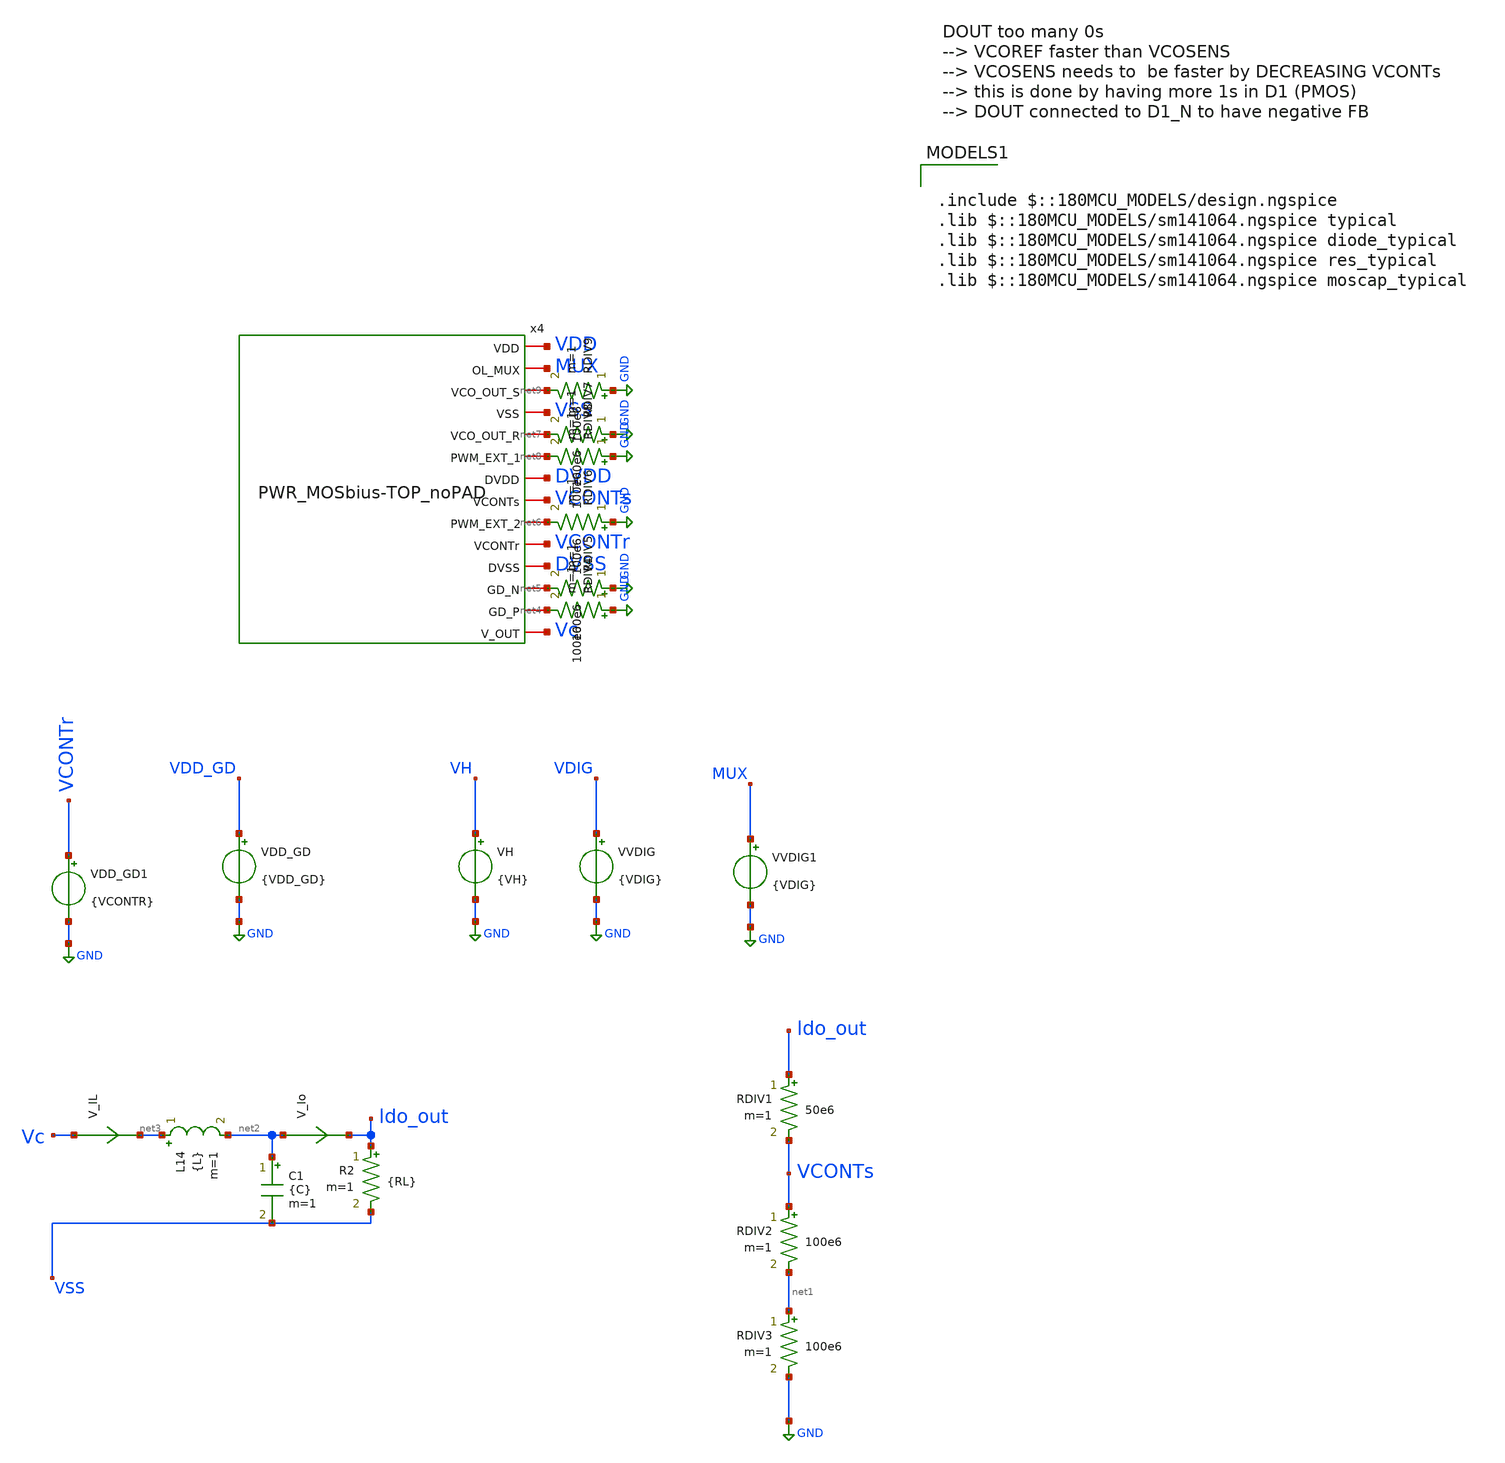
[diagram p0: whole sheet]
** sch_path: xschem/top/tb_TDBuckTOP-IHP-CL_v3p3_NOLnoPAD.sch
**.subckt tb_TDBuckTOP-IHP-CL_v3p3_NOLnoPAD
VH VH GND {VH}
VVDIG VDIG GND {VDIG}
RDIV1 ldo_out VCONTs 50e6 m=1
RDIV2 VCONTs net1 100e6 m=1
RDIV3 net1 GND 100e6 m=1
VDD_GD VDD_GD GND {VDD_GD}
L14 net3 net2 {L} m=1
C1 net2 VSS {C} m=1
V_Io net2 ldo_out 0
.save i(v_io)
V_IL Vc net3 0
.save i(v_il)
R2 ldo_out VSS {RL} m=1
VDD_GD1 VCONTr GND {VCONTR}
VVDIG1 MUX GND {VDIG}
RDIV4 GND net4 100e6 m=1
RDIV5 GND net5 100e6 m=1
RDIV6 GND net6 100e6 m=1
RDIV7 GND net7 100e6 m=1
RDIV8 GND net8 100e6 m=1
RDIV9 GND net9 100e6 m=1
x4 VDD MUX net9 VSS net7 net8 DVDD VCONTs net6 VCONTr DVSS net5 net4 Vc PWR_MOSbius-TOP_noPAD
**** begin user architecture code

.param VDIG = 5
.param VH = 5
.param VDD_GD = 5
.param VCONTR = 2
*LATEST TDBuckLOADS
*300mA
*.param RL = 6
*270mA
*.param RL = 6.67
*240mA
*.param RL = 7.5
*210mA
*.param RL = 8.57
*180mA
*.param RL = 10
*150mA
*.param RL = 12
*120mA
*.param RL = 15
*60mA
*.param RL = 30
*30mA
*.param RL = 60
*15mA
.param RL = 120
*.save v(ldo_out) v(D1) v(D1_N) v(DOUT) v(VCONTr) v(VCONTs) v(V_1r) v(V_1s) v(DOUT_buff) v(DOUT_buffn) v(vh) i(vh) v(vdd_gd) i(vdd_gd) i(v_res) v(VCONTs_OL) v(vcp) v(vcn) i(vldo_out) i(vvdig) i(vvdd)
.save all
vvdd vdd 0 dc 5
vvss vss 0 0
vdvdd dvdd 0 dc 5
vdvss dvss 0 0
*vvconts VCONTs 0 dc 0.61
*.option temp = 200
*.options savecurrents klu method=gear reltol=1e-2 abstol=1e-15 gmin=1e-15
.ic v(VCONTs) = 2
*.ic v(V_1s) = 2
*.ic v(V_2s) = 4
*.ic v(V_1r) = 5
*.ic v(V_2r) = 0
.ic v(x4.V_1s) = 2
.ic v(x4.V_2s) = 4
.ic v(x4.V_1r) = 5
.ic v(x4.V_2r) = 0
.ic v(ldo_out) = 2.5

.control
*tran 2n 1m
*tran 4n 250u
tran 10p 20u uic
*wrdata /foss/designs/TO202406_CMOSVCO_Esm22/xschem/data/dataVSENS_2xCMOSVCOnDFF_v1p1.txt v(V_1s)
*+ tran1.v(V_1s) tran2.v(V_1s) tran3.v(V_1s) tran4.v(V_1s) tran5.v(V_1s) tran6.v(V_1s) tran7.v(V_1s) tran8.v(V_1s)
*+ tran9.v(V_1s) tran10.v(V_1s) tran11.v(V_1s) tran12.v(V_1s) tran13.v(V_1s) tran14.v(V_1s) tran15.v(V_1s)
*+ tran16.v(V_1s) tran17.v(V_1s) tran18.v(V_1s) tran19.v(V_1s)
*wrdata /foss/designs/TO202406_CMOSVCO_Esm22/xschem/data/data_TDBuckTOP-CL_v5p3_RL60.txt tran.v(vh)
*+ tran.i(vh) tran.v(ldo_out) tran.i(vldo_out) tran.v(vh_gd) tran.i(vh_gd) tran.i(vvdig) tran.i(vvdd)
plot v(ldo_out)
plot v(v_res)
plot v(D1) v(D1_N)+5
plot v(DOUT)
plot v(V_1s)+5 v(V_1r)+10
plot v(VCONTr) v(VCONTs)
*plot v(VCONTs_OL)
.endc





*PMOS
.param mult_gd_p = 72
.param w_gd_p = 6.4u
.param l_gd_p = 0.5u
*NMOS
.param mult_gd_n = 72
.param w_gd_n = 2u
.param l_gd_n = 0.6u





.param temp=27
.param mult_M1 = 2000
.param w_M1 =10u
.param l_M1 = 0.5u


.param mult_M2 = 625
.param w_M2 =10u
.param l_M2 =0.6u

*PMOS
.param mult_gd_p = 72
.param w_gd_p = 6.4u
.param l_gd_p = 0.5u
*NMOS
.param mult_gd_n = 72
.param w_gd_n = 2u
.param l_gd_n = 0.6u






*.param L = 550n
*.param R = 16.7
*.param C = 640n
.param L = 220n
*.param C = 1u
.param C = 150n




.include /foss/pdks/gf180mcuD/libs.ref/gf180mcu_fd_sc_mcu9t5v0/spice/gf180mcu_fd_sc_mcu9t5v0.spice
*.include $::180MCU_MODELS/design.ngspice
.include gf180mcu_fd_io__asig_5p0_extracted.spice
.include gf180mcu_fd_io.spice
*.lib $::180MCU_MODELS/sm141064.ngspice typical


.include $::180MCU_MODELS/design.ngspice
.lib $::180MCU_MODELS/sm141064.ngspice typical
.lib $::180MCU_MODELS/sm141064.ngspice diode_typical
.lib $::180MCU_MODELS/sm141064.ngspice res_typical
.lib $::180MCU_MODELS/sm141064.ngspice moscap_typical

**** end user architecture code
**.ends
.GLOBAL GND
.end
